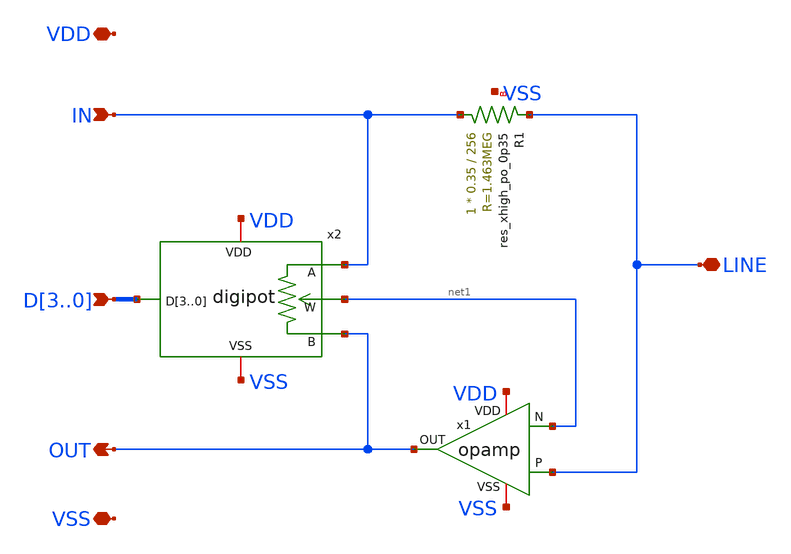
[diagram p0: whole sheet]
** sch_path: xschem/hybrid_ctrl.sch
**.subckt hybrid_ctrl VDD VSS IN OUT LINE D3,D2,D1,D0
*.iopin VDD
*.iopin VSS
*.ipin IN
*.opin OUT
*.iopin LINE
*.ipin D3,D2,D1,D0
x1 VDD OUT LINE net1 VSS opamp
XR1 IN LINE VSS sky130_fd_pr__res_xhigh_po_0p35 L=256 mult=1 m=1
x2 VDD D3 D2 D1 D0 IN net1 OUT VSS digipot
**.ends

* expanding   symbol:  opamp.sym # of pins=5
** sym_path: xschem/opamp.sym
** sch_path: xschem/opamp.sch
.subckt opamp VDD OUT P N VSS
*.iopin VDD
*.iopin VSS
*.ipin P
*.ipin N
*.opin OUT
XR1 net2 VDD VSS sky130_fd_pr__res_xhigh_po_0p35 L=25 mult=1 m=1
XM1 net2 net2 VSS VSS sky130_fd_pr__nfet_g5v0d10v5 L=1 W=2 nf=1 ad='int((1 + 1)/2) * 2 / 1 * 0.29' as='int((1 + 2)/2) * 2 / 1 * 0.29'
+ pd='2*int((1 + 1)/2) * (2 / 1 + 0.29)' ps='2*int((1 + 2)/2) * (2 / 1 + 0.29)' nrd='0.29 / 2 ' nrs='0.29 / 2 '
+ sa=0 sb=0 sd=0 mult=2 m=2
XM7 net1 net1 VDD VDD sky130_fd_pr__pfet_g5v0d10v5 L=1 W=4 nf=1 ad='int((1 + 1)/2) * 4 / 1 * 0.29' as='int((1 + 2)/2) * 4 / 1 * 0.29'
+ pd='2*int((1 + 1)/2) * (4 / 1 + 0.29)' ps='2*int((1 + 2)/2) * (4 / 1 + 0.29)' nrd='0.29 / 4 ' nrs='0.29 / 4 '
+ sa=0 sb=0 sd=0 mult=2 m=2
XM8 OUT net1 VDD VDD sky130_fd_pr__pfet_g5v0d10v5 L=1 W=4 nf=1 ad='int((1 + 1)/2) * 4 / 1 * 0.29' as='int((1 + 2)/2) * 4 / 1 * 0.29'
+ pd='2*int((1 + 1)/2) * (4 / 1 + 0.29)' ps='2*int((1 + 2)/2) * (4 / 1 + 0.29)' nrd='0.29 / 4 ' nrs='0.29 / 4 '
+ sa=0 sb=0 sd=0 mult=2 m=2
XM4 net6 net2 VSS VSS sky130_fd_pr__nfet_g5v0d10v5 L=1 W=2 nf=1 ad='int((1 + 1)/2) * 2 / 1 * 0.29' as='int((1 + 2)/2) * 2 / 1 * 0.29'
+ pd='2*int((1 + 1)/2) * (2 / 1 + 0.29)' ps='2*int((1 + 2)/2) * (2 / 1 + 0.29)' nrd='0.29 / 2 ' nrs='0.29 / 2 '
+ sa=0 sb=0 sd=0 mult=2 m=2
XM5 net1 P net6 VSS sky130_fd_pr__nfet_g5v0d10v5 L=1 W=2 nf=1 ad='int((1 + 1)/2) * 2 / 1 * 0.29' as='int((1 + 2)/2) * 2 / 1 * 0.29'
+ pd='2*int((1 + 1)/2) * (2 / 1 + 0.29)' ps='2*int((1 + 2)/2) * (2 / 1 + 0.29)' nrd='0.29 / 2 ' nrs='0.29 / 2 '
+ sa=0 sb=0 sd=0 mult=2 m=2
XM6 OUT N net6 VSS sky130_fd_pr__nfet_g5v0d10v5 L=1 W=2 nf=1 ad='int((1 + 1)/2) * 2 / 1 * 0.29' as='int((1 + 2)/2) * 2 / 1 * 0.29'
+ pd='2*int((1 + 1)/2) * (2 / 1 + 0.29)' ps='2*int((1 + 2)/2) * (2 / 1 + 0.29)' nrd='0.29 / 2 ' nrs='0.29 / 2 '
+ sa=0 sb=0 sd=0 mult=2 m=2
XM2 net5 net2 VSS VSS sky130_fd_pr__nfet_g5v0d10v5 L=1 W=2 nf=1 ad='int((1 + 1)/2) * 2 / 1 * 0.29' as='int((1 + 2)/2) * 2 / 1 * 0.29'
+ pd='2*int((1 + 1)/2) * (2 / 1 + 0.29)' ps='2*int((1 + 2)/2) * (2 / 1 + 0.29)' nrd='0.29 / 2 ' nrs='0.29 / 2 '
+ sa=0 sb=0 sd=0 mult=2 m=2
XM9 net4 net5 VDD VDD sky130_fd_pr__pfet_g5v0d10v5 L=1 W=4 nf=1 ad='int((1 + 1)/2) * 4 / 1 * 0.29' as='int((1 + 2)/2) * 4 / 1 * 0.29'
+ pd='2*int((1 + 1)/2) * (4 / 1 + 0.29)' ps='2*int((1 + 2)/2) * (4 / 1 + 0.29)' nrd='0.29 / 4 ' nrs='0.29 / 4 '
+ sa=0 sb=0 sd=0 mult=2 m=2
XM3 VDD net5 net5 VDD sky130_fd_pr__pfet_g5v0d10v5 L=1 W=4 nf=1 ad='int((1 + 1)/2) * 4 / 1 * 0.29' as='int((1 + 2)/2) * 4 / 1 * 0.29'
+ pd='2*int((1 + 1)/2) * (4 / 1 + 0.29)' ps='2*int((1 + 2)/2) * (4 / 1 + 0.29)' nrd='0.29 / 4 ' nrs='0.29 / 4 '
+ sa=0 sb=0 sd=0 mult=2 m=2
XM10 net3 P net4 VDD sky130_fd_pr__pfet_g5v0d10v5 L=1 W=4 nf=1 ad='int((1 + 1)/2) * 4 / 1 * 0.29' as='int((1 + 2)/2) * 4 / 1 * 0.29'
+ pd='2*int((1 + 1)/2) * (4 / 1 + 0.29)' ps='2*int((1 + 2)/2) * (4 / 1 + 0.29)' nrd='0.29 / 4 ' nrs='0.29 / 4 '
+ sa=0 sb=0 sd=0 mult=2 m=2
XM11 OUT N net4 VDD sky130_fd_pr__pfet_g5v0d10v5 L=1 W=4 nf=1 ad='int((1 + 1)/2) * 4 / 1 * 0.29' as='int((1 + 2)/2) * 4 / 1 * 0.29'
+ pd='2*int((1 + 1)/2) * (4 / 1 + 0.29)' ps='2*int((1 + 2)/2) * (4 / 1 + 0.29)' nrd='0.29 / 4 ' nrs='0.29 / 4 '
+ sa=0 sb=0 sd=0 mult=2 m=2
XM12 net3 net3 VSS VSS sky130_fd_pr__nfet_g5v0d10v5 L=1 W=2 nf=1 ad='int((1 + 1)/2) * 2 / 1 * 0.29' as='int((1 + 2)/2) * 2 / 1 * 0.29'
+ pd='2*int((1 + 1)/2) * (2 / 1 + 0.29)' ps='2*int((1 + 2)/2) * (2 / 1 + 0.29)' nrd='0.29 / 2 ' nrs='0.29 / 2 '
+ sa=0 sb=0 sd=0 mult=2 m=2
XM13 OUT net3 VSS VSS sky130_fd_pr__nfet_g5v0d10v5 L=1 W=2 nf=1 ad='int((1 + 1)/2) * 2 / 1 * 0.29' as='int((1 + 2)/2) * 2 / 1 * 0.29'
+ pd='2*int((1 + 1)/2) * (2 / 1 + 0.29)' ps='2*int((1 + 2)/2) * (2 / 1 + 0.29)' nrd='0.29 / 2 ' nrs='0.29 / 2 '
+ sa=0 sb=0 sd=0 mult=2 m=2
.ends


* expanding   symbol:  digipot.sym # of pins=6
** sym_path: xschem/digipot.sym
** sch_path: xschem/digipot.sch
.subckt digipot VDD D3 D2 D1 D0 A W B VSS
*.iopin VDD
*.iopin VSS
*.iopin A
*.iopin B
*.iopin W
*.ipin D3,D2,D1,D0
x1 VDD D3 D2 D1 D0 net1[15] net1[14] net1[13] net1[12] net1[11] net1[10] net1[9] net1[8] net1[7]
+ net1[6] net1[5] net1[4] net1[3] net1[2] net1[1] net1[0] VSS decoder4_signed
x2 VDD net1[15] net1[14] net1[13] net1[12] net1[11] net1[10] net1[9] net1[8] net1[7] net1[6] net1[5]
+ net1[4] net1[3] net1[2] net1[1] net1[0] A W B VSS digipot_1hot
.ends


* expanding   symbol:  decoder4_signed.sym # of pins=4
** sym_path: xschem/decoder4_signed.sym
** sch_path: xschem/decoder4_signed.sch
.subckt decoder4_signed VDD D3 D2 D1 D0 U15 U14 U13 U12 U11 U10 U9 U8 U7 U6 U5 U4 U3 U2 U1 U0 VSS
*.iopin VDD
*.iopin VSS
*.opin U15,U14,U13,U12,U11,U10,U9,U8,U7,U6,U5,U4,U3,U2,U1,U0
*.ipin D3,D2,D1,D0
x1 VDD D0 D3 net4 net3 net1 net2 VSS VDD decoder2
x2 VDD D2 D1 U14 U12 U10 U8 VSS net2 decoder2
x3 VDD D2 D1 U6 U4 U2 U0 VSS net1 decoder2
x4 VDD D2 D1 U15 U13 U11 U9 VSS net3 decoder2
x5 VDD D2 D1 U7 U5 U3 U1 VSS net4 decoder2
.ends


* expanding   symbol:  digipot_1hot.sym # of pins=6
** sym_path: xschem/digipot_1hot.sym
** sch_path: xschem/digipot_1hot.sch
.subckt digipot_1hot VDD U15 U14 U13 U12 U11 U10 U9 U8 U7 U6 U5 U4 U3 U2 U1 U0 A W B VSS
*.iopin VDD
*.iopin VSS
*.iopin A
*.iopin B
*.iopin W
*.ipin U15,U14,U13,U12,U11,U10,U9,U8,U7,U6,U5,U4,U3,U2,U1,U0
XR1 A net1 VSS sky130_fd_pr__res_xhigh_po_0p35 L=32 mult=1 m=1
XR2 net1 net2 VSS sky130_fd_pr__res_xhigh_po_0p35 L=32 mult=1 m=1
XR3 net2 net3 VSS sky130_fd_pr__res_xhigh_po_0p35 L=32 mult=1 m=1
XR4 net3 net4 VSS sky130_fd_pr__res_xhigh_po_0p35 L=32 mult=1 m=1
XR5 net4 net5 VSS sky130_fd_pr__res_xhigh_po_0p35 L=32 mult=1 m=1
x1 VDD A W U0 VSS passgate
x2 VDD net1 W U1 VSS passgate
x3 VDD net2 W U2 VSS passgate
x4 VDD net3 W U3 VSS passgate
x5 VDD net4 W U4 VSS passgate
XR6 net5 net6 VSS sky130_fd_pr__res_xhigh_po_0p35 L=32 mult=1 m=1
x6 VDD net5 W U5 VSS passgate
XR7 net6 net7 VSS sky130_fd_pr__res_xhigh_po_0p35 L=32 mult=1 m=1
x7 VDD net6 W U6 VSS passgate
XR8 net8 net7 VSS sky130_fd_pr__res_xhigh_po_0p35 L=32 mult=1 m=1
x8 VDD net7 W U7 VSS passgate
XR9 net8 net9 VSS sky130_fd_pr__res_xhigh_po_0p35 L=32 mult=1 m=1
XR10 net9 net10 VSS sky130_fd_pr__res_xhigh_po_0p35 L=32 mult=1 m=1
XR11 net10 net11 VSS sky130_fd_pr__res_xhigh_po_0p35 L=32 mult=1 m=1
XR12 net11 net12 VSS sky130_fd_pr__res_xhigh_po_0p35 L=32 mult=1 m=1
XR13 net12 net13 VSS sky130_fd_pr__res_xhigh_po_0p35 L=32 mult=1 m=1
x9 VDD net8 W U8 VSS passgate
x10 VDD net9 W U9 VSS passgate
x11 VDD net10 W U10 VSS passgate
x12 VDD net11 W U11 VSS passgate
x13 VDD net12 W U12 VSS passgate
XR14 net13 net14 VSS sky130_fd_pr__res_xhigh_po_0p35 L=32 mult=1 m=1
x14 VDD net13 W U13 VSS passgate
XR15 net14 net15 VSS sky130_fd_pr__res_xhigh_po_0p35 L=32 mult=1 m=1
x15 VDD net14 W U14 VSS passgate
x16 VDD net15 W U15 VSS passgate
XR16 B net15 VSS sky130_fd_pr__res_xhigh_po_0p35 L=32 mult=1 m=1
.ends


* expanding   symbol:  decoder2.sym # of pins=9
** sym_path: xschem/decoder2.sym
** sch_path: xschem/decoder2.sch
.subckt decoder2 VDD D1 D0 U3 U2 U1 U0 VSS EN
*.iopin VDD
*.iopin VSS
*.ipin D0
*.ipin D1
*.opin U0
*.opin U1
*.opin U2
*.opin U3
*.ipin EN
x6 VDD net5 net4 U0 net3 VSS nor3
x7 VDD net5 net1 U1 net3 VSS nor3
x8 VDD net2 net4 U2 net3 VSS nor3
x9 VDD net2 net1 U3 net3 VSS nor3
x1 VDD EN net3 VSS inverter
x2 VDD D0 net1 VSS inverter
x3 VDD net1 net4 VSS inverter
x4 VDD D1 net2 VSS inverter
x5 VDD net2 net5 VSS inverter
.ends


* expanding   symbol:  passgate.sym # of pins=5
** sym_path: xschem/passgate.sym
** sch_path: xschem/passgate.sch
.subckt passgate VDD UA UB EN VSS
*.iopin VSS
*.iopin VDD
*.iopin UA
*.iopin UB
*.ipin EN
XM1 UA EN UB VSS sky130_fd_pr__nfet_g5v0d10v5 L=0.5 W=0.65 nf=1 ad='int((1 + 1)/2) * 0.65 / 1 * 0.29'
+ as='int((1 + 2)/2) * 0.65 / 1 * 0.29' pd='2*int((1 + 1)/2) * (0.65 / 1 + 0.29)' ps='2*int((1 + 2)/2) * (0.65 / 1 + 0.29)'
+ nrd='0.29 / 0.65 ' nrs='0.29 / 0.65 ' sa=0 sb=0 sd=0 mult=1 m=1
XM2 UA net1 UB VDD sky130_fd_pr__pfet_g5v0d10v5 L=0.5 W=1 nf=1 ad='int((1 + 1)/2) * 1 / 1 * 0.29' as='int((1 + 2)/2) * 1 / 1 * 0.29'
+ pd='2*int((1 + 1)/2) * (1 / 1 + 0.29)' ps='2*int((1 + 2)/2) * (1 / 1 + 0.29)' nrd='0.29 / 1 ' nrs='0.29 / 1 '
+ sa=0 sb=0 sd=0 mult=1 m=1
x1 VDD EN net1 VSS inverter
.ends


* expanding   symbol:  nor3.sym # of pins=6
** sym_path: xschem/nor3.sym
** sch_path: xschem/nor3.sch
.subckt nor3 VDD A B OUT C VSS
*.iopin VSS
*.iopin VDD
*.ipin B
*.ipin A
*.ipin C
*.opin OUT
XM2 OUT B VSS VSS sky130_fd_pr__nfet_g5v0d10v5 L=0.5 W=0.65 nf=1 ad='int((1 + 1)/2) * 0.65 / 1 * 0.29'
+ as='int((1 + 2)/2) * 0.65 / 1 * 0.29' pd='2*int((1 + 1)/2) * (0.65 / 1 + 0.29)' ps='2*int((1 + 2)/2) * (0.65 / 1 + 0.29)'
+ nrd='0.29 / 0.65 ' nrs='0.29 / 0.65 ' sa=0 sb=0 sd=0 mult=1 m=1
XM1 OUT A VSS VSS sky130_fd_pr__nfet_g5v0d10v5 L=0.5 W=0.65 nf=1 ad='int((1 + 1)/2) * 0.65 / 1 * 0.29'
+ as='int((1 + 2)/2) * 0.65 / 1 * 0.29' pd='2*int((1 + 1)/2) * (0.65 / 1 + 0.29)' ps='2*int((1 + 2)/2) * (0.65 / 1 + 0.29)'
+ nrd='0.29 / 0.65 ' nrs='0.29 / 0.65 ' sa=0 sb=0 sd=0 mult=1 m=1
XM4 net1 A VDD VDD sky130_fd_pr__pfet_g5v0d10v5 L=0.5 W=1 nf=1 ad='int((1 + 1)/2) * 1 / 1 * 0.29' as='int((1 + 2)/2) * 1 / 1 * 0.29'
+ pd='2*int((1 + 1)/2) * (1 / 1 + 0.29)' ps='2*int((1 + 2)/2) * (1 / 1 + 0.29)' nrd='0.29 / 1 ' nrs='0.29 / 1 '
+ sa=0 sb=0 sd=0 mult=1 m=1
XM3 OUT C VSS VSS sky130_fd_pr__nfet_g5v0d10v5 L=0.5 W=0.65 nf=1 ad='int((1 + 1)/2) * 0.65 / 1 * 0.29'
+ as='int((1 + 2)/2) * 0.65 / 1 * 0.29' pd='2*int((1 + 1)/2) * (0.65 / 1 + 0.29)' ps='2*int((1 + 2)/2) * (0.65 / 1 + 0.29)'
+ nrd='0.29 / 0.65 ' nrs='0.29 / 0.65 ' sa=0 sb=0 sd=0 mult=1 m=1
XM5 net2 B net1 VDD sky130_fd_pr__pfet_g5v0d10v5 L=0.5 W=1 nf=1 ad='int((1 + 1)/2) * 1 / 1 * 0.29' as='int((1 + 2)/2) * 1 / 1 * 0.29'
+ pd='2*int((1 + 1)/2) * (1 / 1 + 0.29)' ps='2*int((1 + 2)/2) * (1 / 1 + 0.29)' nrd='0.29 / 1 ' nrs='0.29 / 1 '
+ sa=0 sb=0 sd=0 mult=1 m=1
XM6 OUT C net2 VDD sky130_fd_pr__pfet_g5v0d10v5 L=0.5 W=1 nf=1 ad='int((1 + 1)/2) * 1 / 1 * 0.29' as='int((1 + 2)/2) * 1 / 1 * 0.29'
+ pd='2*int((1 + 1)/2) * (1 / 1 + 0.29)' ps='2*int((1 + 2)/2) * (1 / 1 + 0.29)' nrd='0.29 / 1 ' nrs='0.29 / 1 '
+ sa=0 sb=0 sd=0 mult=1 m=1
.ends


* expanding   symbol:  inverter.sym # of pins=4
** sym_path: xschem/inverter.sym
** sch_path: xschem/inverter.sch
.subckt inverter VDD IN OUT VSS
*.iopin VSS
*.iopin VDD
*.ipin IN
*.opin OUT
XM1 OUT IN VSS VSS sky130_fd_pr__nfet_g5v0d10v5 L=0.5 W=0.65 nf=1 ad='int((1 + 1)/2) * 0.65 / 1 * 0.29'
+ as='int((1 + 2)/2) * 0.65 / 1 * 0.29' pd='2*int((1 + 1)/2) * (0.65 / 1 + 0.29)' ps='2*int((1 + 2)/2) * (0.65 / 1 + 0.29)'
+ nrd='0.29 / 0.65 ' nrs='0.29 / 0.65 ' sa=0 sb=0 sd=0 mult=1 m=1
XM2 OUT IN VDD VDD sky130_fd_pr__pfet_g5v0d10v5 L=0.5 W=1 nf=1 ad='int((1 + 1)/2) * 1 / 1 * 0.29' as='int((1 + 2)/2) * 1 / 1 * 0.29'
+ pd='2*int((1 + 1)/2) * (1 / 1 + 0.29)' ps='2*int((1 + 2)/2) * (1 / 1 + 0.29)' nrd='0.29 / 1 ' nrs='0.29 / 1 '
+ sa=0 sb=0 sd=0 mult=1 m=1
.ends

.end
